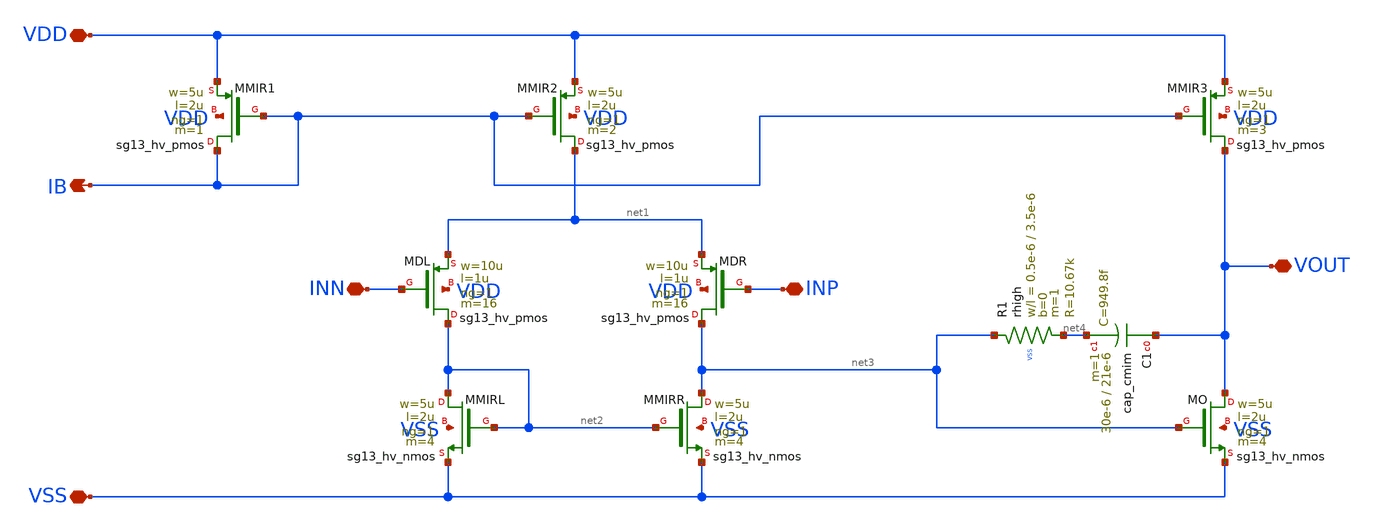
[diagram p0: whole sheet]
** sch_path: ip/bmbg/xschem/bmbgota.sch
**.subckt bmbgota INP INN VOUT IB VDD VSS
*.iopin INP
*.iopin INN
*.iopin VOUT
*.opin IB
*.iopin VDD
*.iopin VSS
XMMIR1 IB IB VDD VDD sg13_hv_pmos w=5u l=2u ng=1 m=1 mm_ok=1
XMMIR2 net1 IB VDD VDD sg13_hv_pmos w=5u l=2u ng=1 m=2 mm_ok=1
XMMIR3 VOUT IB VDD VDD sg13_hv_pmos w=5u l=2u ng=1 m=3 mm_ok=1
XMDL net2 INN net1 VDD sg13_hv_pmos w=10u l=1u ng=1 m=16 mm_ok=1
XMDR net3 INP net1 VDD sg13_hv_pmos w=10u l=1u ng=1 m=16 mm_ok=1
XMMIRR net3 net2 VSS VSS sg13_hv_nmos w=5u l=2u ng=1 m=4 mm_ok=1
XMMIRL net2 net2 VSS VSS sg13_hv_nmos w=5u l=2u ng=1 m=4 mm_ok=1
XMO VOUT net3 VSS VSS sg13_hv_nmos w=5u l=2u ng=1 m=4 mm_ok=1
XC1 VOUT net4 cap_cmim w=30e-6 l=21e-6 m=1 mm_ok=1
XR1 net3 net4 VSS rhigh w=0.5e-6 l=3.5e-6 m=1 b=0 mm_ok=1
**.ends
.end
